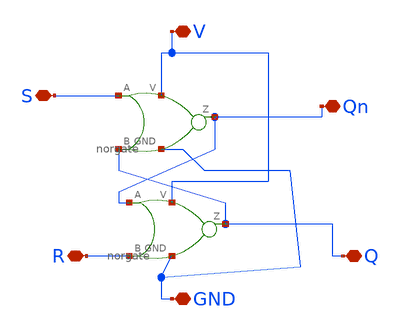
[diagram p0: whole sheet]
** sch_path: SAR_ADC/xschem/spice/symbols/SR_nor.sch
**.subckt SR_nor V GND S R Qn Q
*.iopin V
*.iopin GND
*.iopin S
*.iopin R
*.iopin Qn
*.iopin Q
X1 S Q Qn GND V norgate
X2 Qn R Q GND V norgate
**.ends

* expanding   symbol:  norgate.sym # of pins=5
** sym_path: SAR_ADC/xschem/designs/norgate.sym
** sch_path: SAR_ADC/xschem/designs/norgate.sch
.subckt norgate A B Z GND V
*.iopin GND
*.iopin A
*.iopin B
*.iopin V
*.iopin Z
XM3 V A net2 V pfet_03v3 L=0.28u W=0.22u nf=1 ad='int((nf+1)/2) * W/nf * 0.18u' as='int((nf+2)/2) * W/nf * 0.18u'
+ pd='2*int((nf+1)/2) * (W/nf + 0.18u)' ps='2*int((nf+2)/2) * (W/nf + 0.18u)' nrd='0.18u / W' nrs='0.18u / W'
+ sa=0 sb=0 sd=0 m=1
XM6 net2 B Z V pfet_03v3 L=0.28u W=0.22u nf=1 ad='int((nf+1)/2) * W/nf * 0.18u' as='int((nf+2)/2) * W/nf * 0.18u'
+ pd='2*int((nf+1)/2) * (W/nf + 0.18u)' ps='2*int((nf+2)/2) * (W/nf + 0.18u)' nrd='0.18u / W' nrs='0.18u / W'
+ sa=0 sb=0 sd=0 m=1
XM9 V B net1 V pfet_03v3 L=0.28u W=0.22u nf=1 ad='int((nf+1)/2) * W/nf * 0.18u' as='int((nf+2)/2) * W/nf * 0.18u'
+ pd='2*int((nf+1)/2) * (W/nf + 0.18u)' ps='2*int((nf+2)/2) * (W/nf + 0.18u)' nrd='0.18u / W' nrs='0.18u / W'
+ sa=0 sb=0 sd=0 m=1
XM12 net1 A Z V pfet_03v3 L=0.28u W=0.22u nf=1 ad='int((nf+1)/2) * W/nf * 0.18u' as='int((nf+2)/2) * W/nf * 0.18u'
+ pd='2*int((nf+1)/2) * (W/nf + 0.18u)' ps='2*int((nf+2)/2) * (W/nf + 0.18u)' nrd='0.18u / W' nrs='0.18u / W'
+ sa=0 sb=0 sd=0 m=1
XM2 Z B GND GND nfet_03v3 L=0.28u W=0.22u nf=1 ad='int((nf+1)/2) * W/nf * 0.18u' as='int((nf+2)/2) * W/nf * 0.18u'
+ pd='2*int((nf+1)/2) * (W/nf + 0.18u)' ps='2*int((nf+2)/2) * (W/nf + 0.18u)' nrd='0.18u / W' nrs='0.18u / W'
+ sa=0 sb=0 sd=0 m=1
XM4 Z A GND GND nfet_03v3 L=0.28u W=0.22u nf=1 ad='int((nf+1)/2) * W/nf * 0.18u' as='int((nf+2)/2) * W/nf * 0.18u'
+ pd='2*int((nf+1)/2) * (W/nf + 0.18u)' ps='2*int((nf+2)/2) * (W/nf + 0.18u)' nrd='0.18u / W' nrs='0.18u / W'
+ sa=0 sb=0 sd=0 m=1
.ends

.end
